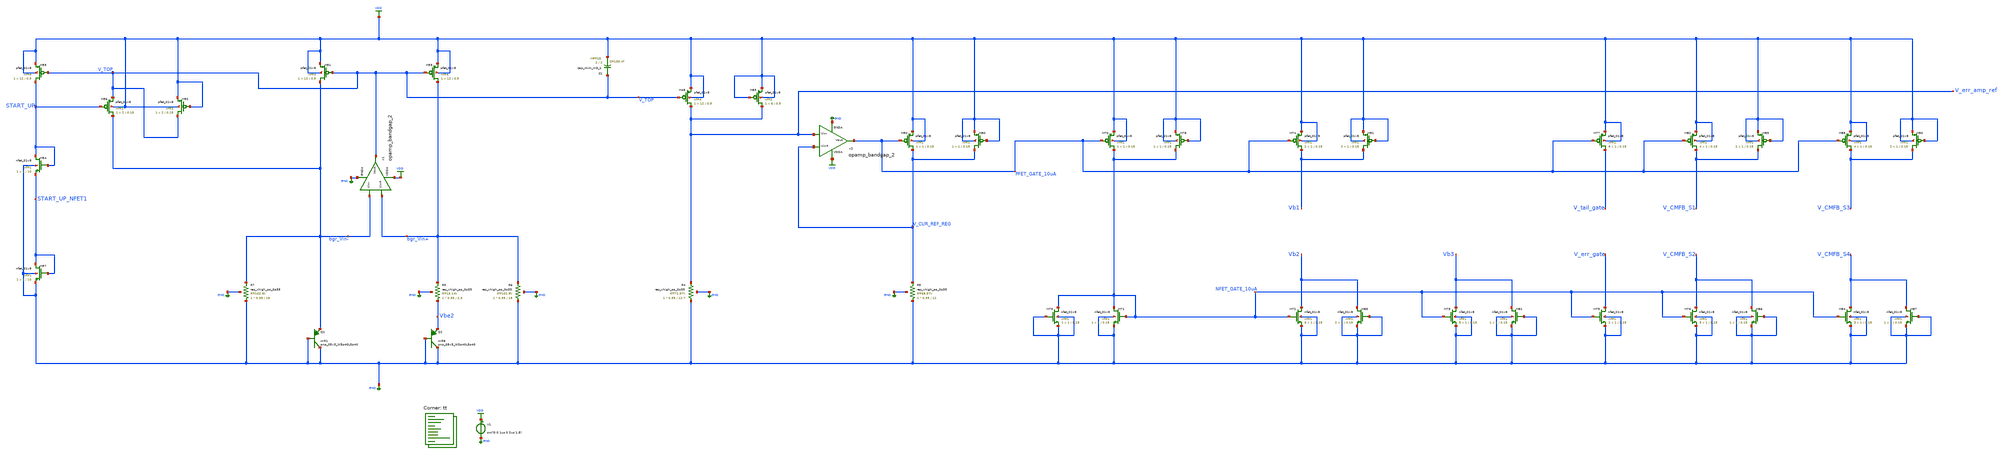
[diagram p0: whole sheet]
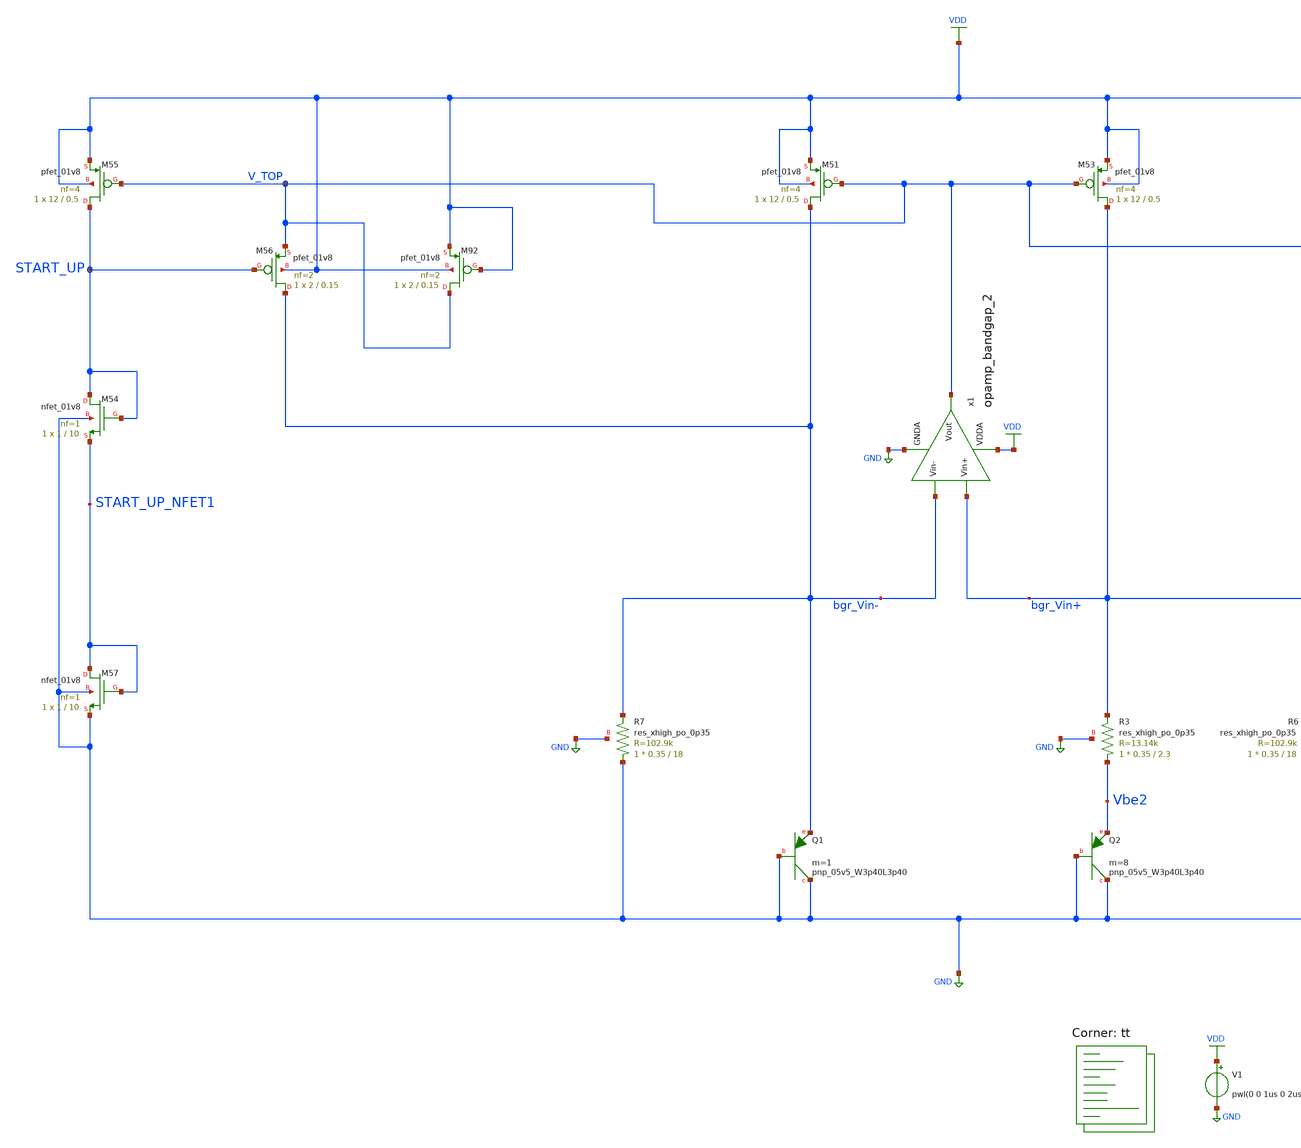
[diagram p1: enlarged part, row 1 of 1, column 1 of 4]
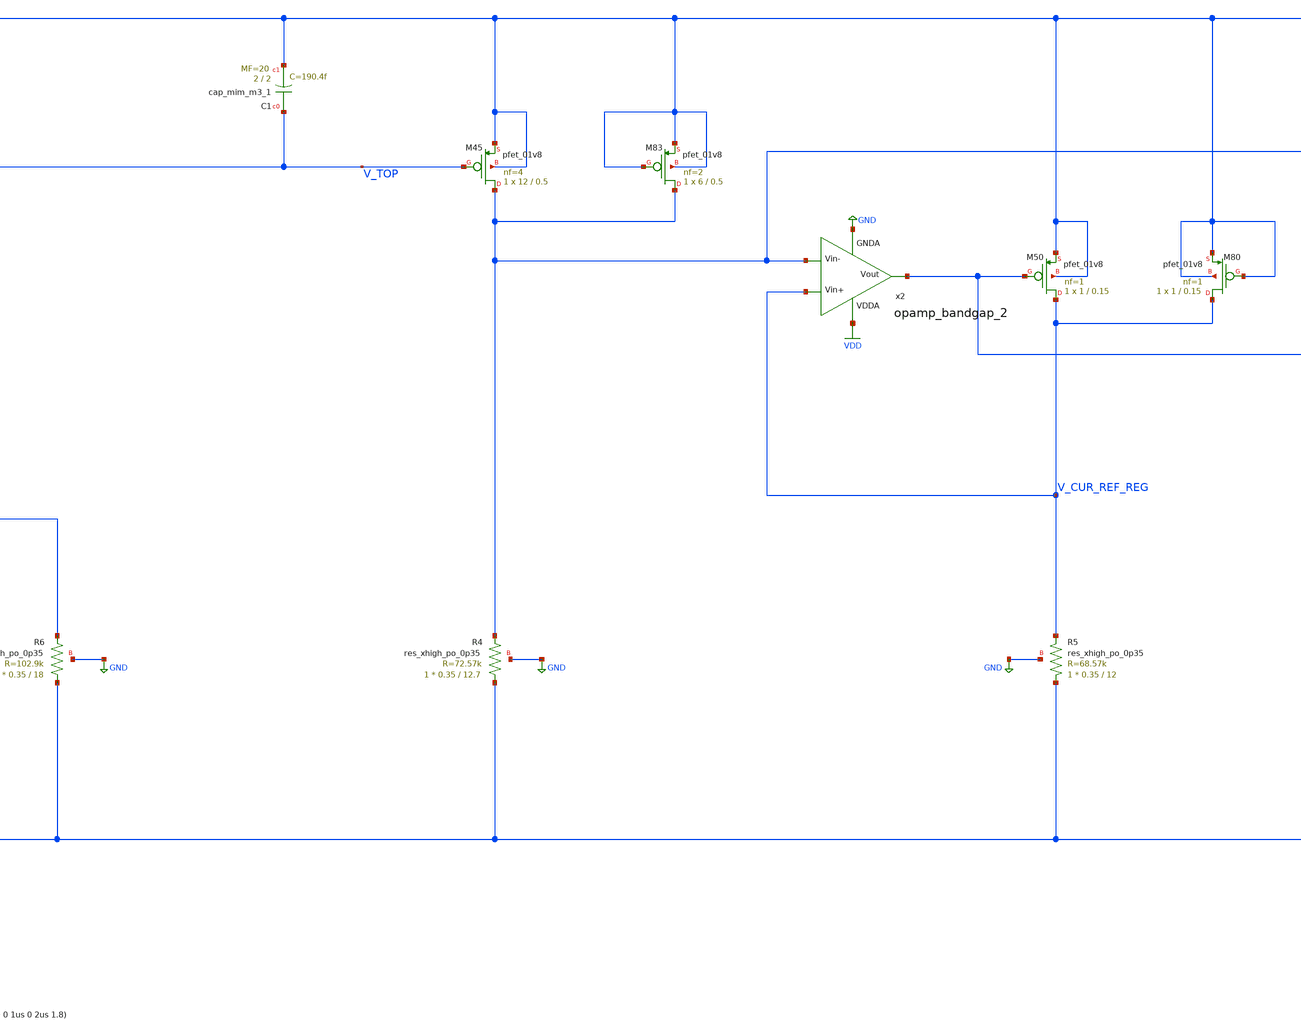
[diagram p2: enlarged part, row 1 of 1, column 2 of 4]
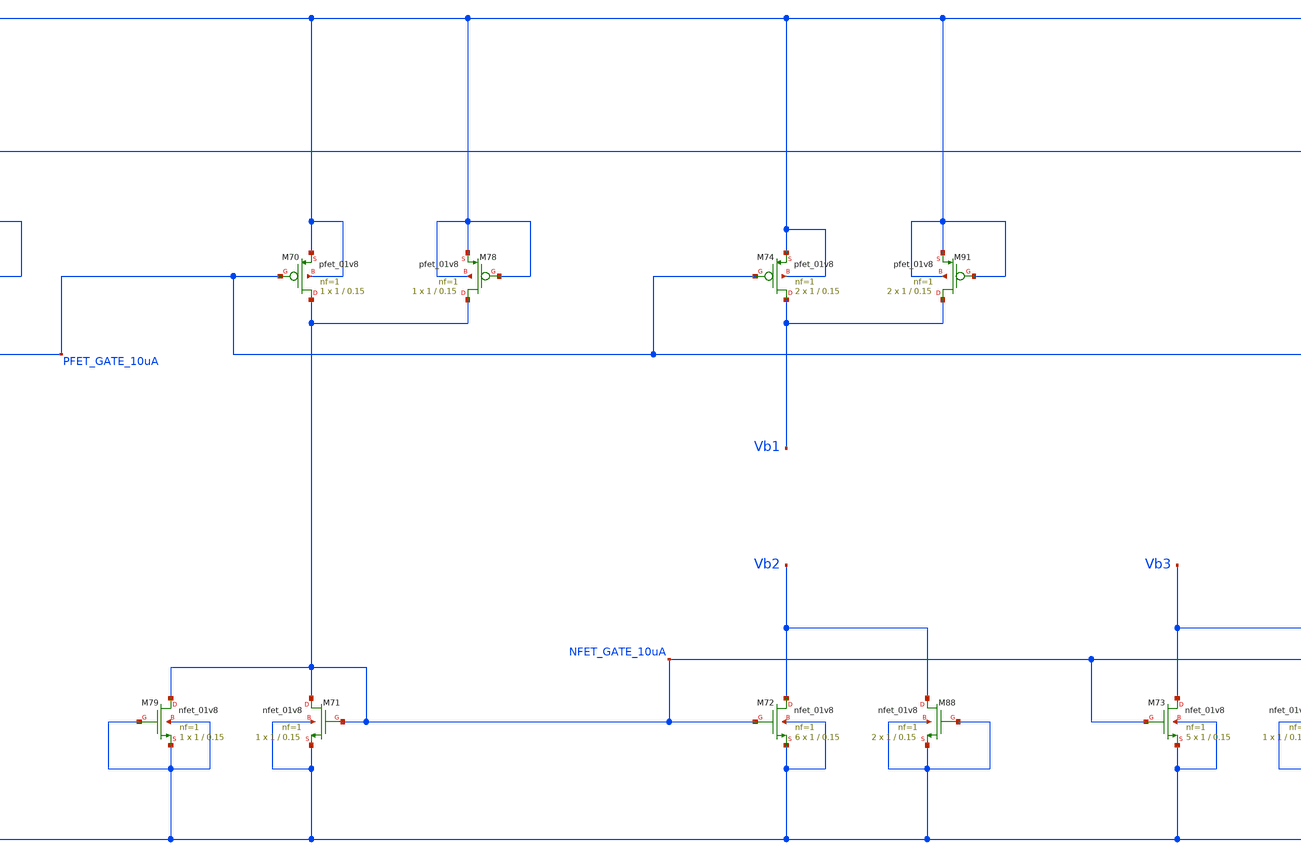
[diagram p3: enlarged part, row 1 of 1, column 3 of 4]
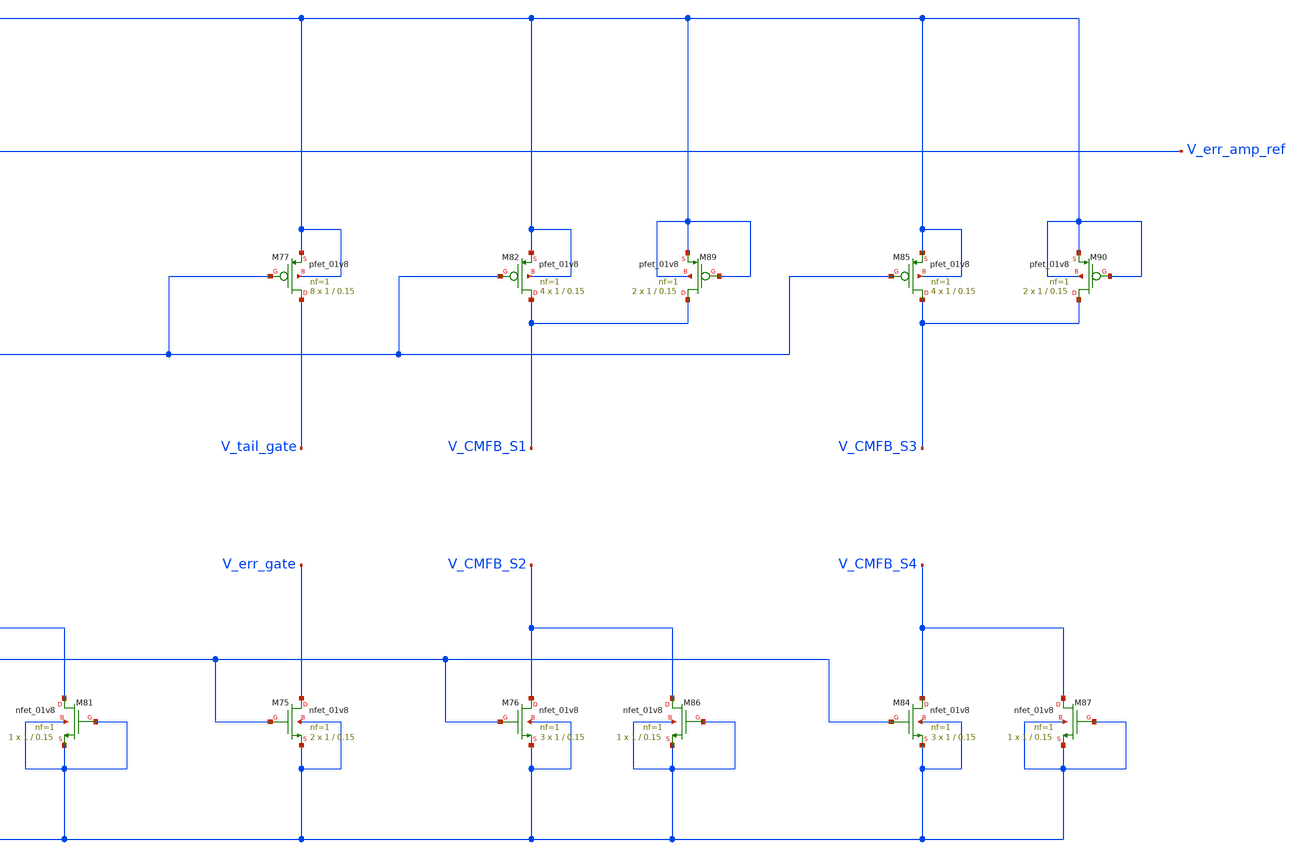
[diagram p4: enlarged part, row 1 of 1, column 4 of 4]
** sch_path: projects/opamp/xschem_ngspice/tb_ref_volt_cur_gen_dummy.sch
**.subckt tb_ref_volt_cur_gen_dummy
V1 VDD GND pwl(0 0 1us 0 2us 1.8)
XM45 V_err_amp_ref V_TOP VDD VDD sky130_fd_pr__pfet_01v8 L=0.5 W=12 nf=4 ad='int((nf+1)/2) * W/nf * 0.29'
+ as='int((nf+2)/2) * W/nf * 0.29' pd='2*int((nf+1)/2) * (W/nf + 0.29)' ps='2*int((nf+2)/2) * (W/nf + 0.29)'
+ nrd='0.29 / W' nrs='0.29 / W' sa=0 sb=0 sd=0 mult=1 m=1
XR4 GND V_err_amp_ref GND sky130_fd_pr__res_xhigh_po_0p35 L=12.7 mult=1 m=1
XR5 GND V_CUR_REF_REG GND sky130_fd_pr__res_xhigh_po_0p35 L=12 mult=1 m=1
XM50 V_CUR_REF_REG PFET_GATE_10uA VDD VDD sky130_fd_pr__pfet_01v8 L=0.15 W=1 nf=1 ad='int((nf+1)/2) * W/nf * 0.29'
+ as='int((nf+2)/2) * W/nf * 0.29' pd='2*int((nf+1)/2) * (W/nf + 0.29)' ps='2*int((nf+2)/2) * (W/nf + 0.29)'
+ nrd='0.29 / W' nrs='0.29 / W' sa=0 sb=0 sd=0 mult=1 m=1
XC1 V_TOP VDD sky130_fd_pr__cap_mim_m3_1 W=2 L=2 MF=20 m=20
XQ1 GND GND bgr_Vin- sky130_fd_pr__pnp_05v5_W3p40L3p40 m=1
XQ2 GND GND Vbe2 sky130_fd_pr__pnp_05v5_W3p40L3p40 m=8
XM51 bgr_Vin- V_TOP VDD VDD sky130_fd_pr__pfet_01v8 L=0.5 W=12 nf=4 ad='int((nf+1)/2) * W/nf * 0.29'
+ as='int((nf+2)/2) * W/nf * 0.29' pd='2*int((nf+1)/2) * (W/nf + 0.29)' ps='2*int((nf+2)/2) * (W/nf + 0.29)'
+ nrd='0.29 / W' nrs='0.29 / W' sa=0 sb=0 sd=0 mult=1 m=1
XM53 bgr_Vin+ V_TOP VDD VDD sky130_fd_pr__pfet_01v8 L=0.5 W=12 nf=4 ad='int((nf+1)/2) * W/nf * 0.29'
+ as='int((nf+2)/2) * W/nf * 0.29' pd='2*int((nf+1)/2) * (W/nf + 0.29)' ps='2*int((nf+2)/2) * (W/nf + 0.29)'
+ nrd='0.29 / W' nrs='0.29 / W' sa=0 sb=0 sd=0 mult=1 m=1
XR3 Vbe2 bgr_Vin+ GND sky130_fd_pr__res_xhigh_po_0p35 L=2.3 mult=1 m=1
XR6 GND bgr_Vin+ GND sky130_fd_pr__res_xhigh_po_0p35 L=18 mult=1 m=1
XR7 GND bgr_Vin- GND sky130_fd_pr__res_xhigh_po_0p35 L=18 mult=1 m=1
XM54 START_UP START_UP START_UP_NFET1 GND sky130_fd_pr__nfet_01v8 L=10 W=1 nf=1 ad='int((nf+1)/2) * W/nf * 0.29'
+ as='int((nf+2)/2) * W/nf * 0.29' pd='2*int((nf+1)/2) * (W/nf + 0.29)' ps='2*int((nf+2)/2) * (W/nf + 0.29)'
+ nrd='0.29 / W' nrs='0.29 / W' sa=0 sb=0 sd=0 mult=1 m=1
XM55 START_UP V_TOP VDD VDD sky130_fd_pr__pfet_01v8 L=0.5 W=12 nf=4 ad='int((nf+1)/2) * W/nf * 0.29'
+ as='int((nf+2)/2) * W/nf * 0.29' pd='2*int((nf+1)/2) * (W/nf + 0.29)' ps='2*int((nf+2)/2) * (W/nf + 0.29)'
+ nrd='0.29 / W' nrs='0.29 / W' sa=0 sb=0 sd=0 mult=1 m=1
XM56 bgr_Vin- START_UP V_TOP VDD sky130_fd_pr__pfet_01v8 L=0.15 W=2 nf=2 ad='int((nf+1)/2) * W/nf * 0.29'
+ as='int((nf+2)/2) * W/nf * 0.29' pd='2*int((nf+1)/2) * (W/nf + 0.29)' ps='2*int((nf+2)/2) * (W/nf + 0.29)'
+ nrd='0.29 / W' nrs='0.29 / W' sa=0 sb=0 sd=0 mult=1 m=1
XM57 START_UP_NFET1 START_UP_NFET1 GND GND sky130_fd_pr__nfet_01v8 L=10 W=1 nf=1 ad='int((nf+1)/2) * W/nf * 0.29'
+ as='int((nf+2)/2) * W/nf * 0.29' pd='2*int((nf+1)/2) * (W/nf + 0.29)' ps='2*int((nf+2)/2) * (W/nf + 0.29)'
+ nrd='0.29 / W' nrs='0.29 / W' sa=0 sb=0 sd=0 mult=1 m=1
x1 VDD V_TOP bgr_Vin- bgr_Vin+ GND opamp_bandgap_2
x2 VDD PFET_GATE_10uA V_err_amp_ref V_CUR_REF_REG GND opamp_bandgap_2
XM70 NFET_GATE_10uA PFET_GATE_10uA VDD VDD sky130_fd_pr__pfet_01v8 L=0.15 W=1 nf=1 ad='int((nf+1)/2) * W/nf * 0.29'
+ as='int((nf+2)/2) * W/nf * 0.29' pd='2*int((nf+1)/2) * (W/nf + 0.29)' ps='2*int((nf+2)/2) * (W/nf + 0.29)'
+ nrd='0.29 / W' nrs='0.29 / W' sa=0 sb=0 sd=0 mult=1 m=1
XM71 NFET_GATE_10uA NFET_GATE_10uA GND GND sky130_fd_pr__nfet_01v8 L=0.15 W=1 nf=1 ad='int((nf+1)/2) * W/nf * 0.29'
+ as='int((nf+2)/2) * W/nf * 0.29' pd='2*int((nf+1)/2) * (W/nf + 0.29)' ps='2*int((nf+2)/2) * (W/nf + 0.29)'
+ nrd='0.29 / W' nrs='0.29 / W' sa=0 sb=0 sd=0 mult=1 m=1
XM72 Vb2 NFET_GATE_10uA GND GND sky130_fd_pr__nfet_01v8 L=0.15 W=1 nf=1 ad='int((nf+1)/2) * W/nf * 0.29'
+ as='int((nf+2)/2) * W/nf * 0.29' pd='2*int((nf+1)/2) * (W/nf + 0.29)' ps='2*int((nf+2)/2) * (W/nf + 0.29)'
+ nrd='0.29 / W' nrs='0.29 / W' sa=0 sb=0 sd=0 mult=6 m=6
XM73 Vb3 NFET_GATE_10uA GND GND sky130_fd_pr__nfet_01v8 L=0.15 W=1 nf=1 ad='int((nf+1)/2) * W/nf * 0.29'
+ as='int((nf+2)/2) * W/nf * 0.29' pd='2*int((nf+1)/2) * (W/nf + 0.29)' ps='2*int((nf+2)/2) * (W/nf + 0.29)'
+ nrd='0.29 / W' nrs='0.29 / W' sa=0 sb=0 sd=0 mult=5 m=5
XM74 Vb1 PFET_GATE_10uA VDD VDD sky130_fd_pr__pfet_01v8 L=0.15 W=1 nf=1 ad='int((nf+1)/2) * W/nf * 0.29'
+ as='int((nf+2)/2) * W/nf * 0.29' pd='2*int((nf+1)/2) * (W/nf + 0.29)' ps='2*int((nf+2)/2) * (W/nf + 0.29)'
+ nrd='0.29 / W' nrs='0.29 / W' sa=0 sb=0 sd=0 mult=2 m=2
XM75 V_err_gate NFET_GATE_10uA GND GND sky130_fd_pr__nfet_01v8 L=0.15 W=1 nf=1 ad='int((nf+1)/2) * W/nf * 0.29'
+ as='int((nf+2)/2) * W/nf * 0.29' pd='2*int((nf+1)/2) * (W/nf + 0.29)' ps='2*int((nf+2)/2) * (W/nf + 0.29)'
+ nrd='0.29 / W' nrs='0.29 / W' sa=0 sb=0 sd=0 mult=2 m=2
XM76 V_CMFB_S2 NFET_GATE_10uA GND GND sky130_fd_pr__nfet_01v8 L=0.15 W=1 nf=1 ad='int((nf+1)/2) * W/nf * 0.29'
+ as='int((nf+2)/2) * W/nf * 0.29' pd='2*int((nf+1)/2) * (W/nf + 0.29)' ps='2*int((nf+2)/2) * (W/nf + 0.29)'
+ nrd='0.29 / W' nrs='0.29 / W' sa=0 sb=0 sd=0 mult=3 m=3
XM77 V_tail_gate PFET_GATE_10uA VDD VDD sky130_fd_pr__pfet_01v8 L=0.15 W=1 nf=1 ad='int((nf+1)/2) * W/nf * 0.29'
+ as='int((nf+2)/2) * W/nf * 0.29' pd='2*int((nf+1)/2) * (W/nf + 0.29)' ps='2*int((nf+2)/2) * (W/nf + 0.29)'
+ nrd='0.29 / W' nrs='0.29 / W' sa=0 sb=0 sd=0 mult=8 m=8
XM78 NFET_GATE_10uA VDD VDD VDD sky130_fd_pr__pfet_01v8 L=0.15 W=1 nf=1 ad='int((nf+1)/2) * W/nf * 0.29'
+ as='int((nf+2)/2) * W/nf * 0.29' pd='2*int((nf+1)/2) * (W/nf + 0.29)' ps='2*int((nf+2)/2) * (W/nf + 0.29)'
+ nrd='0.29 / W' nrs='0.29 / W' sa=0 sb=0 sd=0 mult=1 m=1
XM79 NFET_GATE_10uA GND GND GND sky130_fd_pr__nfet_01v8 L=0.15 W=1 nf=1 ad='int((nf+1)/2) * W/nf * 0.29'
+ as='int((nf+2)/2) * W/nf * 0.29' pd='2*int((nf+1)/2) * (W/nf + 0.29)' ps='2*int((nf+2)/2) * (W/nf + 0.29)'
+ nrd='0.29 / W' nrs='0.29 / W' sa=0 sb=0 sd=0 mult=1 m=1
XM80 V_CUR_REF_REG VDD VDD VDD sky130_fd_pr__pfet_01v8 L=0.15 W=1 nf=1 ad='int((nf+1)/2) * W/nf * 0.29'
+ as='int((nf+2)/2) * W/nf * 0.29' pd='2*int((nf+1)/2) * (W/nf + 0.29)' ps='2*int((nf+2)/2) * (W/nf + 0.29)'
+ nrd='0.29 / W' nrs='0.29 / W' sa=0 sb=0 sd=0 mult=1 m=1
XM81 Vb3 GND GND GND sky130_fd_pr__nfet_01v8 L=0.15 W=1 nf=1 ad='int((nf+1)/2) * W/nf * 0.29' as='int((nf+2)/2) * W/nf * 0.29'
+ pd='2*int((nf+1)/2) * (W/nf + 0.29)' ps='2*int((nf+2)/2) * (W/nf + 0.29)' nrd='0.29 / W' nrs='0.29 / W'
+ sa=0 sb=0 sd=0 mult=1 m=1
XM82 V_CMFB_S1 PFET_GATE_10uA VDD VDD sky130_fd_pr__pfet_01v8 L=0.15 W=1 nf=1 ad='int((nf+1)/2) * W/nf * 0.29'
+ as='int((nf+2)/2) * W/nf * 0.29' pd='2*int((nf+1)/2) * (W/nf + 0.29)' ps='2*int((nf+2)/2) * (W/nf + 0.29)'
+ nrd='0.29 / W' nrs='0.29 / W' sa=0 sb=0 sd=0 mult=4 m=4
XM83 V_err_amp_ref VDD VDD VDD sky130_fd_pr__pfet_01v8 L=0.5 W=6 nf=2 ad='int((nf+1)/2) * W/nf * 0.29'
+ as='int((nf+2)/2) * W/nf * 0.29' pd='2*int((nf+1)/2) * (W/nf + 0.29)' ps='2*int((nf+2)/2) * (W/nf + 0.29)'
+ nrd='0.29 / W' nrs='0.29 / W' sa=0 sb=0 sd=0 mult=1 m=1
XM84 V_CMFB_S4 NFET_GATE_10uA GND GND sky130_fd_pr__nfet_01v8 L=0.15 W=1 nf=1 ad='int((nf+1)/2) * W/nf * 0.29'
+ as='int((nf+2)/2) * W/nf * 0.29' pd='2*int((nf+1)/2) * (W/nf + 0.29)' ps='2*int((nf+2)/2) * (W/nf + 0.29)'
+ nrd='0.29 / W' nrs='0.29 / W' sa=0 sb=0 sd=0 mult=3 m=3
XM85 V_CMFB_S3 PFET_GATE_10uA VDD VDD sky130_fd_pr__pfet_01v8 L=0.15 W=1 nf=1 ad='int((nf+1)/2) * W/nf * 0.29'
+ as='int((nf+2)/2) * W/nf * 0.29' pd='2*int((nf+1)/2) * (W/nf + 0.29)' ps='2*int((nf+2)/2) * (W/nf + 0.29)'
+ nrd='0.29 / W' nrs='0.29 / W' sa=0 sb=0 sd=0 mult=4 m=4
XM86 V_CMFB_S2 GND GND GND sky130_fd_pr__nfet_01v8 L=0.15 W=1 nf=1 ad='int((nf+1)/2) * W/nf * 0.29' as='int((nf+2)/2) * W/nf * 0.29'
+ pd='2*int((nf+1)/2) * (W/nf + 0.29)' ps='2*int((nf+2)/2) * (W/nf + 0.29)' nrd='0.29 / W' nrs='0.29 / W'
+ sa=0 sb=0 sd=0 mult=1 m=1
XM87 V_CMFB_S4 GND GND GND sky130_fd_pr__nfet_01v8 L=0.15 W=1 nf=1 ad='int((nf+1)/2) * W/nf * 0.29' as='int((nf+2)/2) * W/nf * 0.29'
+ pd='2*int((nf+1)/2) * (W/nf + 0.29)' ps='2*int((nf+2)/2) * (W/nf + 0.29)' nrd='0.29 / W' nrs='0.29 / W'
+ sa=0 sb=0 sd=0 mult=1 m=1
XM88 Vb2 GND GND GND sky130_fd_pr__nfet_01v8 L=0.15 W=1 nf=1 ad='int((nf+1)/2) * W/nf * 0.29' as='int((nf+2)/2) * W/nf * 0.29'
+ pd='2*int((nf+1)/2) * (W/nf + 0.29)' ps='2*int((nf+2)/2) * (W/nf + 0.29)' nrd='0.29 / W' nrs='0.29 / W'
+ sa=0 sb=0 sd=0 mult=2 m=2
XM89 V_CMFB_S1 VDD VDD VDD sky130_fd_pr__pfet_01v8 L=0.15 W=1 nf=1 ad='int((nf+1)/2) * W/nf * 0.29' as='int((nf+2)/2) * W/nf * 0.29'
+ pd='2*int((nf+1)/2) * (W/nf + 0.29)' ps='2*int((nf+2)/2) * (W/nf + 0.29)' nrd='0.29 / W' nrs='0.29 / W'
+ sa=0 sb=0 sd=0 mult=2 m=2
XM90 V_CMFB_S3 VDD VDD VDD sky130_fd_pr__pfet_01v8 L=0.15 W=1 nf=1 ad='int((nf+1)/2) * W/nf * 0.29' as='int((nf+2)/2) * W/nf * 0.29'
+ pd='2*int((nf+1)/2) * (W/nf + 0.29)' ps='2*int((nf+2)/2) * (W/nf + 0.29)' nrd='0.29 / W' nrs='0.29 / W'
+ sa=0 sb=0 sd=0 mult=2 m=2
XM91 Vb1 VDD VDD VDD sky130_fd_pr__pfet_01v8 L=0.15 W=1 nf=1 ad='int((nf+1)/2) * W/nf * 0.29' as='int((nf+2)/2) * W/nf * 0.29'
+ pd='2*int((nf+1)/2) * (W/nf + 0.29)' ps='2*int((nf+2)/2) * (W/nf + 0.29)' nrd='0.29 / W' nrs='0.29 / W'
+ sa=0 sb=0 sd=0 mult=2 m=2
XM92 V_TOP VDD VDD VDD sky130_fd_pr__pfet_01v8 L=0.15 W=2 nf=2 ad='int((nf+1)/2) * W/nf * 0.29' as='int((nf+2)/2) * W/nf * 0.29'
+ pd='2*int((nf+1)/2) * (W/nf + 0.29)' ps='2*int((nf+2)/2) * (W/nf + 0.29)' nrd='0.29 / W' nrs='0.29 / W'
+ sa=0 sb=0 sd=0 mult=1 m=1
**** begin user architecture code
.lib $::SKYWATER_MODELS/sky130.lib.spice tt



* ngspice commands


.option method=gear
.option wnflag=1
.option savecurrents
* .temp =140

.save @m.xm1.msky130_fd_pr__pfet_01v8[gm] @m.xm1.msky130_fd_pr__pfet_01v8[vth] @m.xm1.msky130_fd_pr__pfet_01v8[vgs] @m.xm1.msky130_fd_pr__pfet_01v8[vds] @m.xm2.msky130_fd_pr__pfet_01v8[gm] @m.xm2.msky130_fd_pr__pfet_01v8[vth] @m.xm2.msky130_fd_pr__pfet_01v8[vgs] @m.xm2.msky130_fd_pr__pfet_01v8[vds] @m.xm3.msky130_fd_pr__pfet_01v8[gm] @m.xm4.msky130_fd_pr__pfet_01v8[gm] @m.xm4.msky130_fd_pr__pfet_01v8[vth] @m.xm5.msky130_fd_pr__nfet_01v8[gm] @m.xm5.msky130_fd_pr__nfet_01v8[vth] @m.xm6.msky130_fd_pr__pfet_01v8[gm] @m.xm6.msky130_fd_pr__pfet_01v8[vth] @m.xm7.msky130_fd_pr__nfet_01v8[gm] @m.xm7.msky130_fd_pr__nfet_01v8[vth] @m.xm8.msky130_fd_pr__nfet_01v8[gm] @m.xm8.msky130_fd_pr__nfet_01v8[vth] @m.xm9.msky130_fd_pr__nfet_01v8[gm] @m.xm9.msky130_fd_pr__nfet_01v8[vth] @m.x1.xm1.msky130_fd_pr__nfet_01v8[gm] @m.x1.xm2.msky130_fd_pr__nfet_01v8[gm] @m.x1.xm3.msky130_fd_pr__nfet_01v8[gm] @m.x1.xm4.msky130_fd_pr__nfet_01v8[gm] @m.x1.xm5.msky130_fd_pr__pfet_01v8[gm] @m.x1.xm6.msky130_fd_pr__nfet_01v8[gm] @m.x1.xm7.msky130_fd_pr__pfet_01v8[gm]

* .ic v(vin-) = 0.8
* .ic v(vin+) = 0.8
* .ic v(v_top) = 1.8

.control

    save all
    * dc temp -40 120 5 V1 1.6 2.0 0.05
    * dc V1 1.7 1.9 0.001 temp -40 120 40
    * dc V1 0.0 2.0 0.02 temp -40 120 20
    * dc V1 0 2.0 0.02
    tran 0.4ns 5us
    remzerovec
    write tb_ref_volt_cur_gen_dummy.raw
.endc




**** end user architecture code
**.ends

* expanding   symbol:
*+  /foss/designs/my_design/projects/bandgapref/xschem_ngspice/new_files/opamp_bandgap_2.sym # of pins=5
** sym_path: projects/bandgapref/xschem_ngspice/new_files/opamp_bandgap_2.sym
** sch_path: projects/bandgapref/xschem_ngspice/new_files/opamp_bandgap_2.sch
.subckt opamp_bandgap_2 VDDA Vout Vin- Vin+ GNDA
*.ipin Vin+
*.opin Vout
*.ipin Vin-
*.ipin GNDA
*.ipin VDDA
XM1 V_p VDDA GNDA GNDA sky130_fd_pr__nfet_01v8 L=5 W=2.5 nf=1 ad='int((nf+1)/2) * W/nf * 0.29' as='int((nf+2)/2) * W/nf * 0.29'
+ pd='2*int((nf+1)/2) * (W/nf + 0.29)' ps='2*int((nf+2)/2) * (W/nf + 0.29)' nrd='0.29 / W' nrs='0.29 / W'
+ sa=0 sb=0 sd=0 mult=1 m=1
XM2 V_mirror Vin- V_p GNDA sky130_fd_pr__nfet_01v8 L=0.2 W=2.5 nf=1 ad='int((nf+1)/2) * W/nf * 0.29'
+ as='int((nf+2)/2) * W/nf * 0.29' pd='2*int((nf+1)/2) * (W/nf + 0.29)' ps='2*int((nf+2)/2) * (W/nf + 0.29)'
+ nrd='0.29 / W' nrs='0.29 / W' sa=0 sb=0 sd=0 mult=1 m=1
XM3 1st_Vout Vin+ V_p GNDA sky130_fd_pr__nfet_01v8 L=0.2 W=2.5 nf=1 ad='int((nf+1)/2) * W/nf * 0.29'
+ as='int((nf+2)/2) * W/nf * 0.29' pd='2*int((nf+1)/2) * (W/nf + 0.29)' ps='2*int((nf+2)/2) * (W/nf + 0.29)'
+ nrd='0.29 / W' nrs='0.29 / W' sa=0 sb=0 sd=0 mult=1 m=1
XM5 V_mirror V_mirror VDDA VDDA sky130_fd_pr__pfet_01v8 L=0.2 W=6 nf=2 ad='int((nf+1)/2) * W/nf * 0.29'
+ as='int((nf+2)/2) * W/nf * 0.29' pd='2*int((nf+1)/2) * (W/nf + 0.29)' ps='2*int((nf+2)/2) * (W/nf + 0.29)'
+ nrd='0.29 / W' nrs='0.29 / W' sa=0 sb=0 sd=0 mult=1 m=1
XM6 1st_Vout V_mirror VDDA VDDA sky130_fd_pr__pfet_01v8 L=0.2 W=6 nf=2 ad='int((nf+1)/2) * W/nf * 0.29'
+ as='int((nf+2)/2) * W/nf * 0.29' pd='2*int((nf+1)/2) * (W/nf + 0.29)' ps='2*int((nf+2)/2) * (W/nf + 0.29)'
+ nrd='0.29 / W' nrs='0.29 / W' sa=0 sb=0 sd=0 mult=1 m=1
XM4 Vout VDDA GNDA GNDA sky130_fd_pr__nfet_01v8 L=5 W=2.5 nf=1 ad='int((nf+1)/2) * W/nf * 0.29' as='int((nf+2)/2) * W/nf * 0.29'
+ pd='2*int((nf+1)/2) * (W/nf + 0.29)' ps='2*int((nf+2)/2) * (W/nf + 0.29)' nrd='0.29 / W' nrs='0.29 / W'
+ sa=0 sb=0 sd=0 mult=1 m=1
XM7 Vout 1st_Vout VDDA VDDA sky130_fd_pr__pfet_01v8 L=0.2 W=6 nf=2 ad='int((nf+1)/2) * W/nf * 0.29' as='int((nf+2)/2) * W/nf * 0.29'
+ pd='2*int((nf+1)/2) * (W/nf + 0.29)' ps='2*int((nf+2)/2) * (W/nf + 0.29)' nrd='0.29 / W' nrs='0.29 / W'
+ sa=0 sb=0 sd=0 mult=1 m=1
XC1 1st_Vout cap_res sky130_fd_pr__cap_mim_m3_1 W=2 L=2 MF=20 m=20
XM8 Vout VDDA VDDA VDDA sky130_fd_pr__pfet_01v8 L=0.2 W=1 nf=1 ad='int((nf+1)/2) * W/nf * 0.29' as='int((nf+2)/2) * W/nf * 0.29'
+ pd='2*int((nf+1)/2) * (W/nf + 0.29)' ps='2*int((nf+2)/2) * (W/nf + 0.29)' nrd='0.29 / W' nrs='0.29 / W'
+ sa=0 sb=0 sd=0 mult=2 m=2
XR2 Vout cap_res GNDA sky130_fd_pr__res_high_po_0p35 L=2.05 mult=1 m=1
.ends

.GLOBAL GND
.GLOBAL VDD
.end
